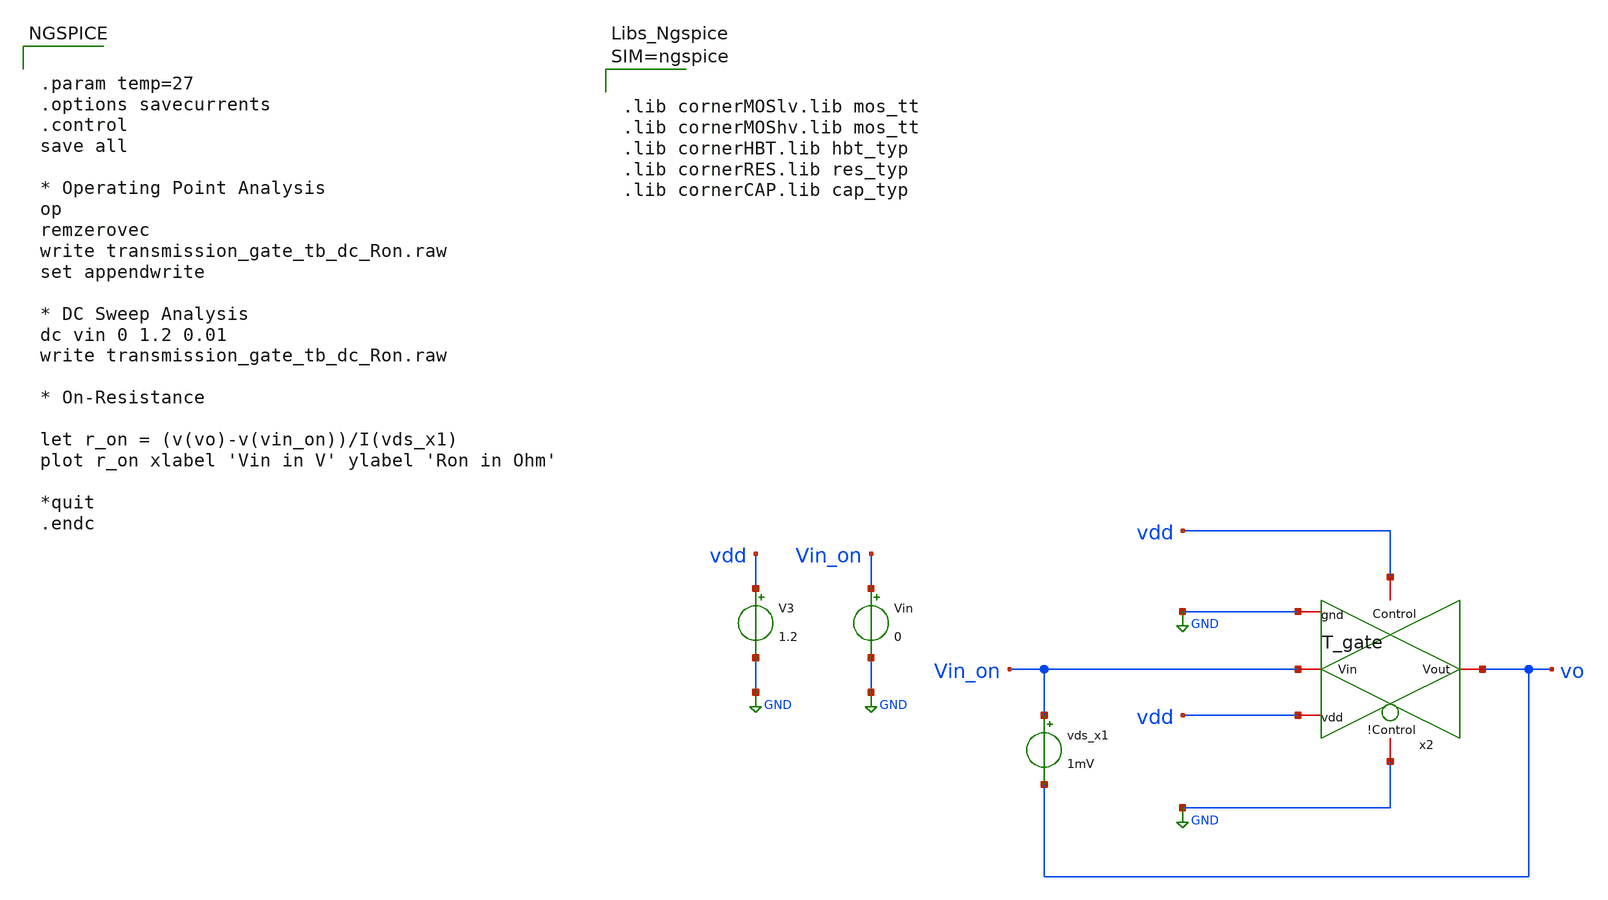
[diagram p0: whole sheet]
** sch_path: xschem/T_gate_tb_dc_Ron.sch
**.subckt T_gate_tb_dc_Ron
x2 GND Vin_on vo GND vdd vdd T_gate
Vin Vin_on GND 0
V3 vdd GND 1.2
vds_x1 Vin_on vo 1mV
**** begin user architecture code


.param temp=27
.options savecurrents
.control
save all

* Operating Point Analysis
op
remzerovec
write transmission_gate_tb_dc_Ron.raw
set appendwrite

* DC Sweep Analysis
dc vin 0 1.2 0.01
write transmission_gate_tb_dc_Ron.raw

* On-Resistance

let r_on = (v(vo)-v(vin_on))/I(vds_x1)
plot r_on xlabel 'Vin in V' ylabel 'Ron in Ohm'

*quit
.endc




.lib cornerMOSlv.lib mos_tt
.lib cornerMOShv.lib mos_tt
.lib cornerHBT.lib hbt_typ
.lib cornerRES.lib res_typ
.lib cornerCAP.lib cap_typ



**** end user architecture code
**.ends

* expanding   symbol:
*+  /home/designer/shared/IHP-AnalogAcademy/modules/module_3_8_bit_SAR_ADC/part_2_digital_comps/T_gate/schematic/T_gate.sym # of pins=6
** sym_path: /home/designer/shared/IHP-AnalogAcademy/modules/module_3_8_bit_SAR_ADC/part_2_digital_comps/T_gate/schematic/T_gate.sym
** sch_path: /home/designer/shared/IHP-AnalogAcademy/modules/module_3_8_bit_SAR_ADC/part_2_digital_comps/T_gate/schematic/T_gate.sch
.subckt T_gate !Control Vin Vout gnd Control vdd
*.iopin Vout
*.iopin Vin
*.iopin !Control
*.iopin Control
*.iopin gnd
*.iopin vdd
XM1 Vin Control Vout gnd sg13_lv_nmos w=1u l=0.13u ng=1 m=1 mm_ok=1
XM2 Vout !Control Vin vdd sg13_lv_pmos w=3u l=0.13u ng=1 m=1 mm_ok=1
.ends

.GLOBAL GND
.end
